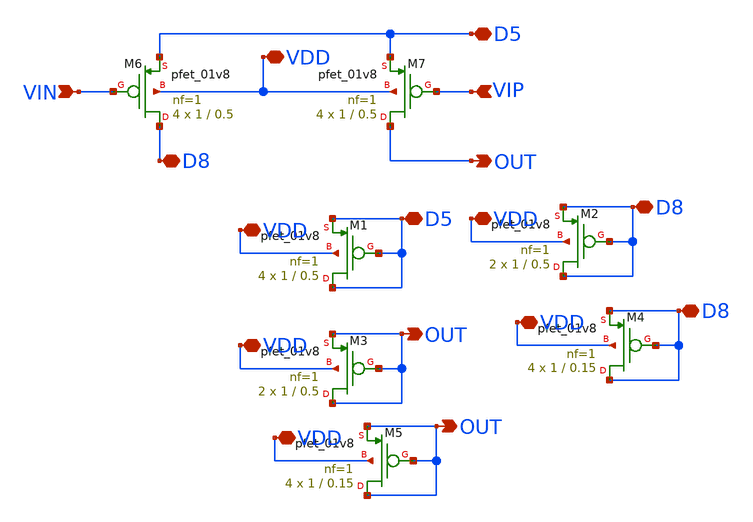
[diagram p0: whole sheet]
** sch_path: opamp/mag/pmos_out.sch
**.subckt pmos_out VIP VIN D8 D5 VDD OUT D5 VDD D8 OUT VDD VDD D8 VDD OUT VDD
*.ipin VIP
*.ipin VIN
*.iopin D8
*.iopin D5
*.iopin VDD
*.opin OUT
*.iopin D5
*.iopin VDD
*.iopin D8
*.opin OUT
*.iopin VDD
*.iopin VDD
*.iopin D8
*.iopin VDD
*.opin OUT
*.iopin VDD
XM6 D8 VIN D5 VDD sky130_fd_pr__pfet_01v8 L=0.5 W=1 nf=1 ad='int((nf+1)/2) * W/nf * 0.29' as='int((nf+2)/2) * W/nf * 0.29'
+ pd='2*int((nf+1)/2) * (W/nf + 0.29)' ps='2*int((nf+2)/2) * (W/nf + 0.29)' nrd='0.29 / W' nrs='0.29 / W'
+ sa=0 sb=0 sd=0 mult=4 m=4
XM7 OUT VIP D5 VDD sky130_fd_pr__pfet_01v8 L=0.5 W=1 nf=1 ad='int((nf+1)/2) * W/nf * 0.29' as='int((nf+2)/2) * W/nf * 0.29'
+ pd='2*int((nf+1)/2) * (W/nf + 0.29)' ps='2*int((nf+2)/2) * (W/nf + 0.29)' nrd='0.29 / W' nrs='0.29 / W'
+ sa=0 sb=0 sd=0 mult=4 m=4
XM1 D5 D5 D5 VDD sky130_fd_pr__pfet_01v8 L=0.5 W=1 nf=1 ad='int((nf+1)/2) * W/nf * 0.29' as='int((nf+2)/2) * W/nf * 0.29'
+ pd='2*int((nf+1)/2) * (W/nf + 0.29)' ps='2*int((nf+2)/2) * (W/nf + 0.29)' nrd='0.29 / W' nrs='0.29 / W'
+ sa=0 sb=0 sd=0 mult=4 m=4
XM2 D8 D8 D8 VDD sky130_fd_pr__pfet_01v8 L=0.5 W=1 nf=1 ad='int((nf+1)/2) * W/nf * 0.29' as='int((nf+2)/2) * W/nf * 0.29'
+ pd='2*int((nf+1)/2) * (W/nf + 0.29)' ps='2*int((nf+2)/2) * (W/nf + 0.29)' nrd='0.29 / W' nrs='0.29 / W'
+ sa=0 sb=0 sd=0 mult=2 m=2
XM3 OUT OUT OUT VDD sky130_fd_pr__pfet_01v8 L=0.5 W=1 nf=1 ad='int((nf+1)/2) * W/nf * 0.29' as='int((nf+2)/2) * W/nf * 0.29'
+ pd='2*int((nf+1)/2) * (W/nf + 0.29)' ps='2*int((nf+2)/2) * (W/nf + 0.29)' nrd='0.29 / W' nrs='0.29 / W'
+ sa=0 sb=0 sd=0 mult=2 m=2
XM4 D8 D8 D8 VDD sky130_fd_pr__pfet_01v8 L=0.15 W=1 nf=1 ad='int((nf+1)/2) * W/nf * 0.29' as='int((nf+2)/2) * W/nf * 0.29'
+ pd='2*int((nf+1)/2) * (W/nf + 0.29)' ps='2*int((nf+2)/2) * (W/nf + 0.29)' nrd='0.29 / W' nrs='0.29 / W'
+ sa=0 sb=0 sd=0 mult=4 m=4
XM5 OUT OUT OUT VDD sky130_fd_pr__pfet_01v8 L=0.15 W=1 nf=1 ad='int((nf+1)/2) * W/nf * 0.29' as='int((nf+2)/2) * W/nf * 0.29'
+ pd='2*int((nf+1)/2) * (W/nf + 0.29)' ps='2*int((nf+2)/2) * (W/nf + 0.29)' nrd='0.29 / W' nrs='0.29 / W'
+ sa=0 sb=0 sd=0 mult=4 m=4
**.ends
.end
